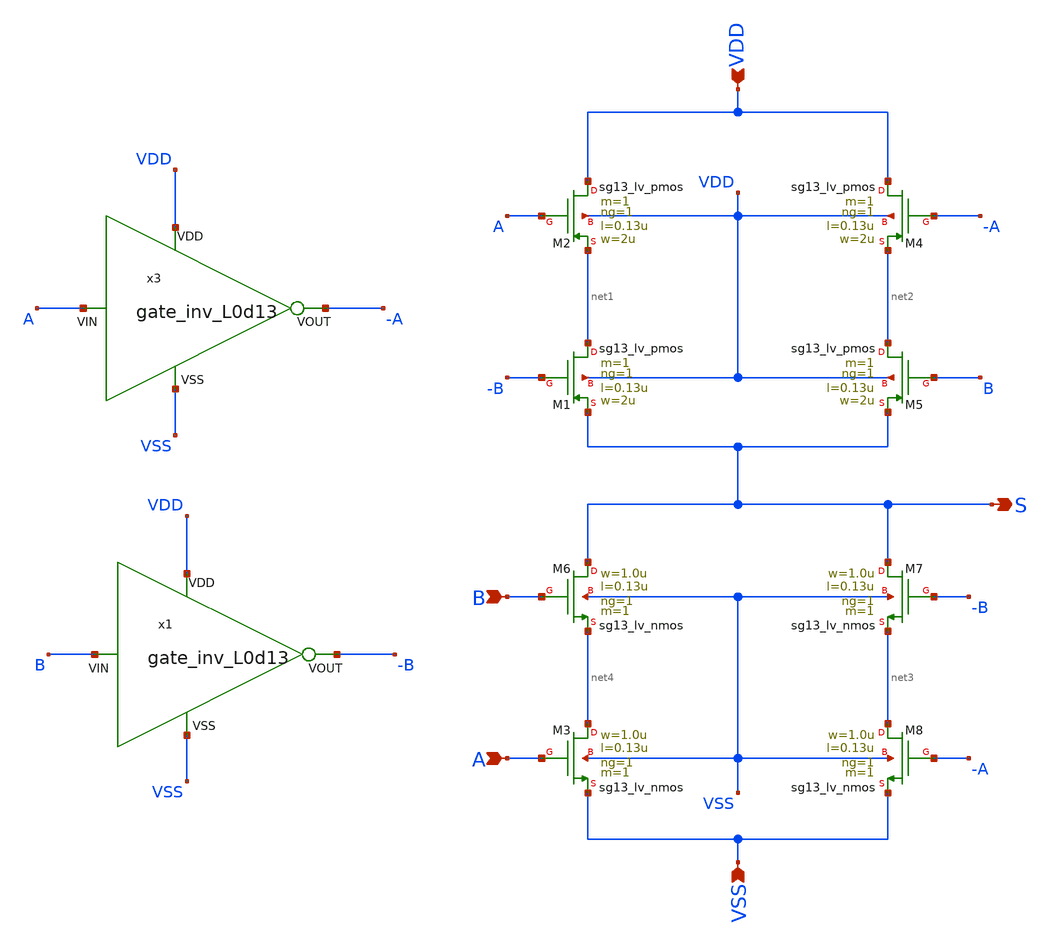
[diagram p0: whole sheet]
** sch_path: work/gate_xor/xschem/gate_xor.sch
**.subckt gate_xor VSS B A VDD S
*.ipin VSS
*.ipin B
*.ipin A
*.ipin VDD
*.opin S
XM2 VDD A net1 VDD sg13_lv_pmos w=2u l=0.13u ng=1 m=1 mm_ok=1
XM1 net1 -B S VDD sg13_lv_pmos w=2u l=0.13u ng=1 m=1 mm_ok=1
XM4 VDD -A net2 VDD sg13_lv_pmos w=2u l=0.13u ng=1 m=1 mm_ok=1
XM5 net2 B S VDD sg13_lv_pmos w=2u l=0.13u ng=1 m=1 mm_ok=1
XM6 S B net4 VSS sg13_lv_nmos w=1.0u l=0.13u ng=1 m=1 mm_ok=1
XM3 net4 A VSS VSS sg13_lv_nmos w=1.0u l=0.13u ng=1 m=1 mm_ok=1
XM7 S -B net3 VSS sg13_lv_nmos w=1.0u l=0.13u ng=1 m=1 mm_ok=1
XM8 net3 -A VSS VSS sg13_lv_nmos w=1.0u l=0.13u ng=1 m=1 mm_ok=1
x3 VDD A -A VSS gate_inv_L0d13
x1 VDD B -B VSS gate_inv_L0d13
**.ends

* expanding   symbol:
*+  /foss/designs/chipathon_2025/designs/ihp-sg13g2/gate_inv_L0d13/xschem/gate_inv_L0d13.sym # of pins=4
** sym_path: /foss/designs/chipathon_2025/designs/ihp-sg13g2/gate_inv_L0d13/xschem/gate_inv_L0d13.sym
** sch_path: /foss/designs/chipathon_2025/designs/ihp-sg13g2/gate_inv_L0d13/xschem/gate_inv_L0d13.sch
.subckt gate_inv_L0d13 VDD VIN VOUT VSS
*.ipin VDD
*.ipin VSS
*.ipin VIN
*.opin VOUT
XM2 VDD VIN VOUT VDD sg13_lv_pmos w=2u l=0.13u ng=1 m=1 mm_ok=1
XM1 VOUT VIN VSS VSS sg13_lv_nmos w=1.0u l=0.13u ng=1 m=1 mm_ok=1
.ends

.end
